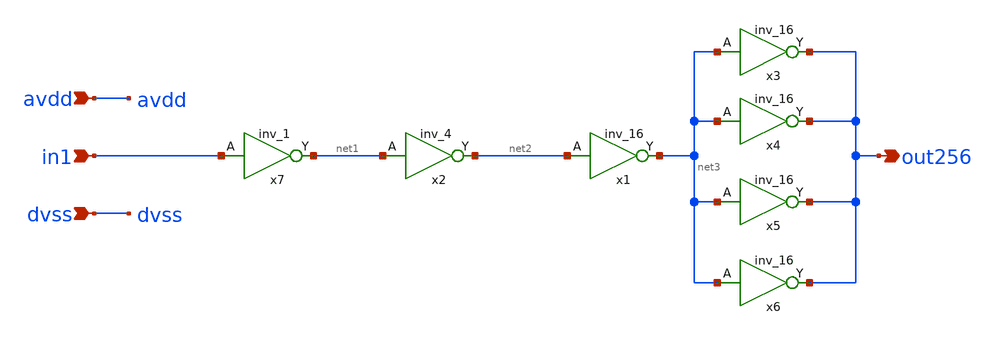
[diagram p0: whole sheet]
** sch_path: xschem/hvbuff1_256.sch
**.subckt hvbuff1_256 avdd in1 dvss out256
*.ipin avdd
*.ipin in1
*.ipin dvss
*.opin out256
x2 net1 dvss dvss avdd avdd net2 sky130_fd_sc_hvl__inv_4
x1 net2 dvss dvss avdd avdd net3 sky130_fd_sc_hvl__inv_16
x3 net3 dvss dvss avdd avdd out256 sky130_fd_sc_hvl__inv_16
x4 net3 dvss dvss avdd avdd out256 sky130_fd_sc_hvl__inv_16
x5 net3 dvss dvss avdd avdd out256 sky130_fd_sc_hvl__inv_16
x6 net3 dvss dvss avdd avdd out256 sky130_fd_sc_hvl__inv_16
x7 in1 dvss dvss avdd avdd net1 sky130_fd_sc_hvl__inv_1
**.ends
.end
